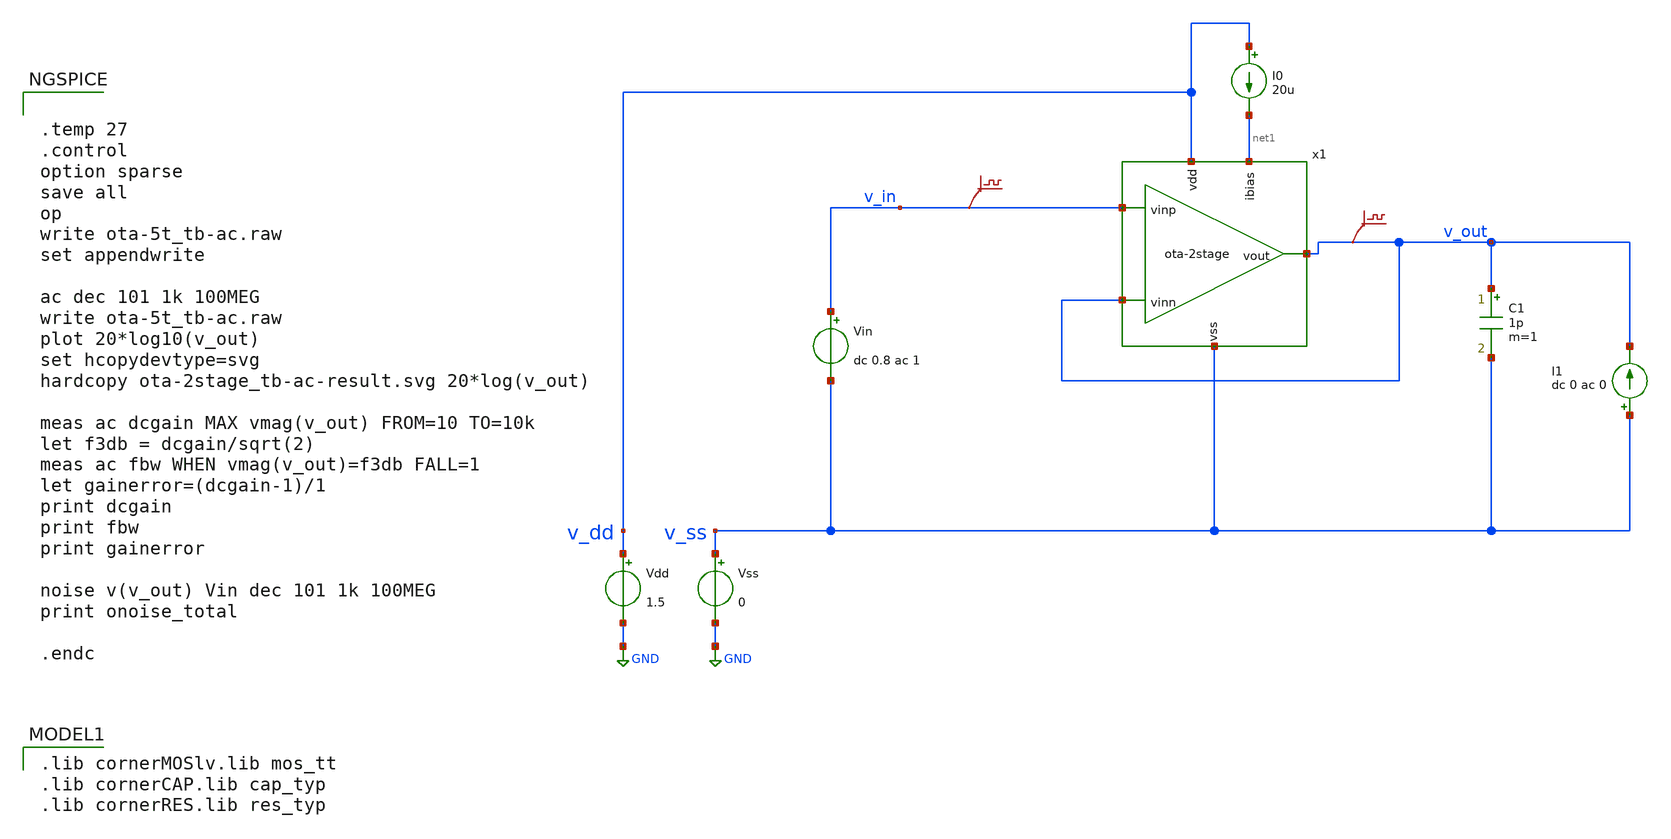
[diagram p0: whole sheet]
** sch_path: xschem/ota-2stage_tb-ac.sch
**.subckt ota-2stage_tb-ac
Vdd v_dd GND 1.5
Vss v_ss GND 0
C1 v_out v_ss 1p m=1
Vin v_in v_ss dc 0.8 ac 1
I0 v_dd net1 20u
.save v(v_in)
.save v(v_out)
I1 v_ss v_out dc 0 ac 0
x1 v_dd net1 v_out v_out v_in v_ss ota-2stage
**** begin user architecture code


.temp 27
.control
option sparse
save all
op
write ota-5t_tb-ac.raw
set appendwrite

ac dec 101 1k 100MEG
write ota-5t_tb-ac.raw
plot 20*log10(v_out)
set hcopydevtype=svg
hardcopy ota-2stage_tb-ac-result.svg 20*log(v_out)

meas ac dcgain MAX vmag(v_out) FROM=10 TO=10k
let f3db = dcgain/sqrt(2)
meas ac fbw WHEN vmag(v_out)=f3db FALL=1
let gainerror=(dcgain-1)/1
print dcgain
print fbw
print gainerror

noise v(v_out) Vin dec 101 1k 100MEG
print onoise_total

.endc


 .lib cornerMOSlv.lib mos_tt
.lib cornerCAP.lib cap_typ
.lib cornerRES.lib res_typ

**** end user architecture code
**.ends
.GLOBAL GND
.end
